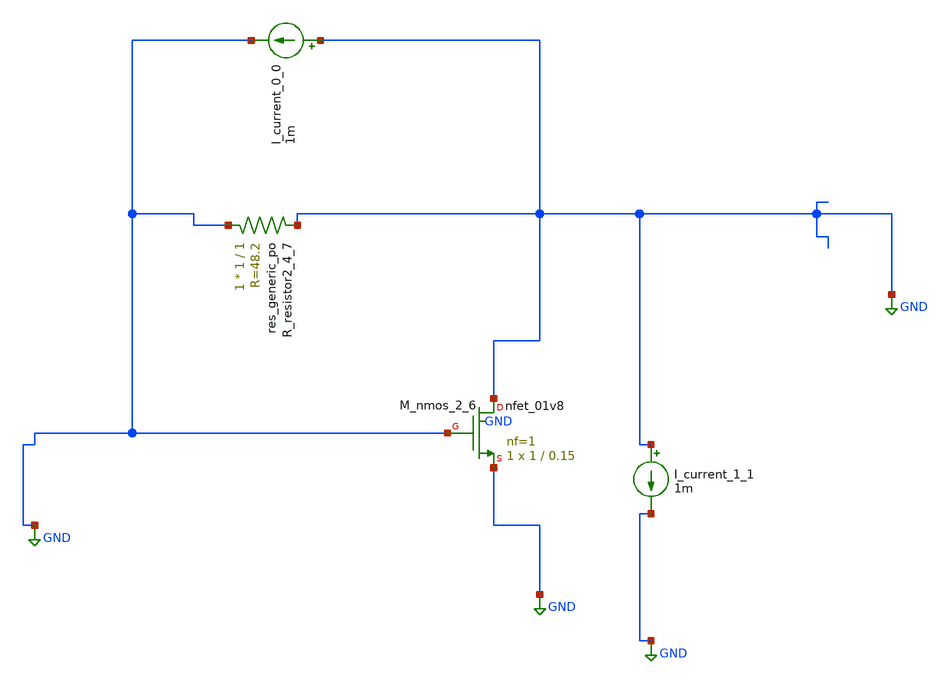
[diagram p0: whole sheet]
** sch_path: schematics/AMSNet/446.sch
**.subckt 446
I_current_0_0 GND GND 1m
I_current_1_1 GND GND 1m
XM_nmos_2_6 GND GND GND GND sky130_fd_pr__nfet_01v8 L=0.15 W=1 nf=1 ad='int((1 + 1)/2) * 1 / 1 * 0.29'
+ as='int((1 + 2)/2) * 1 / 1 * 0.29' pd='2*int((1 + 1)/2) * (1 / 1 + 0.29)' ps='2*int((1 + 2)/2) * (1 / 1 + 0.29)'
+ nrd='0.29 / 1 ' nrs='0.29 / 1 ' sa=0 sb=0 sd=0 mult=1 m=1
XR_resistor2_4_7 GND GND sky130_fd_pr__res_generic_po W=1 L=1 m=1
**.ends
.GLOBAL GND
.end
